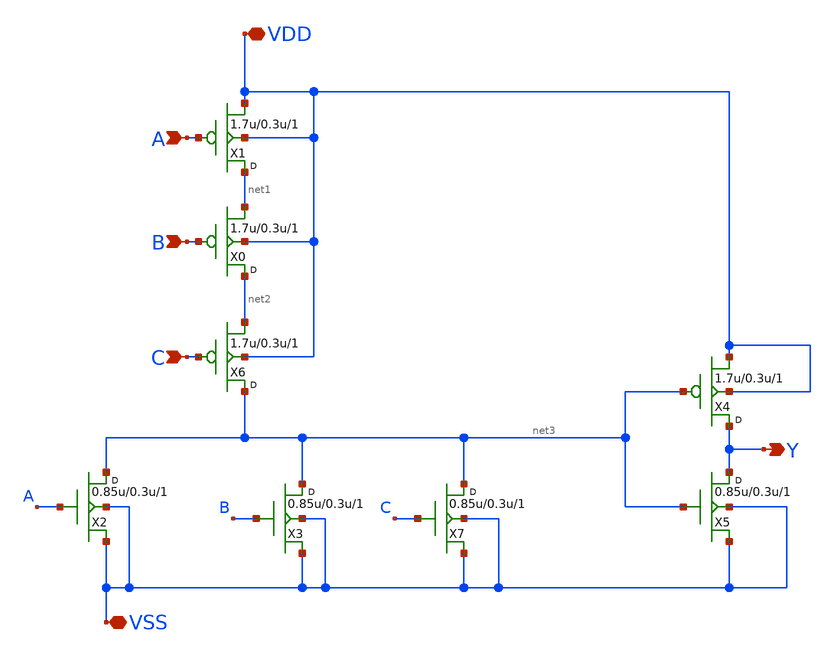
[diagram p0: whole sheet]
** sch_path: designs/libs/core_digital/gf180mcu_osu_sc_gp12t3v3/cells/or3/gf180mcu_osu_sc_gp12t3v3__or3_1.sch
**.subckt gf180mcu_osu_sc_gp12t3v3__or3_1 A B C Y VDD VSS
*.ipin A
*.ipin B
*.ipin C
*.opin Y
*.iopin VDD
*.iopin VSS
X1 net1 A VDD VDD pfet_03v3 w=1.7u l=0.3u m=1
X0 net2 B net1 VDD pfet_03v3 w=1.7u l=0.3u m=1
X6 net3 C net2 VDD pfet_03v3 w=1.7u l=0.3u m=1
X2 net3 A VSS VSS nfet_03v3 w=0.85u l=0.3u m=1
X3 net3 B VSS VSS nfet_03v3 w=0.85u l=0.3u m=1
X7 net3 C VSS VSS nfet_03v3 w=0.85u l=0.3u m=1
X4 Y net3 VDD VDD pfet_03v3 w=1.7u l=0.3u m=1
X5 Y net3 VSS VSS nfet_03v3 w=0.85u l=0.3u m=1
**.ends
.end
